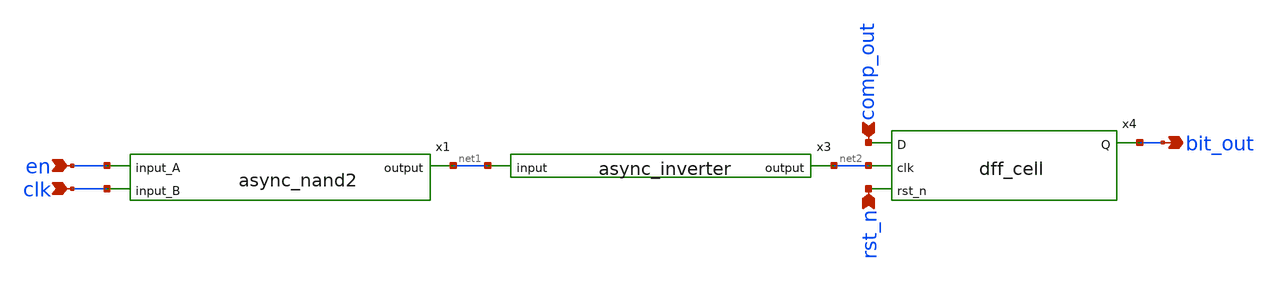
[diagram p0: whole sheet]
** sch_path: xschem/sar_adc/bit_reg.sch
**.subckt bit_reg en clk bit_out comp_out rst_n
*.ipin en
*.ipin clk
*.opin bit_out
*.ipin comp_out
*.ipin rst_n
x1 en net1 clk async_nand2
x3 net2 net1 async_inverter
x4 comp_out net2 rst_n bit_out dff_cell
**.ends
.end
